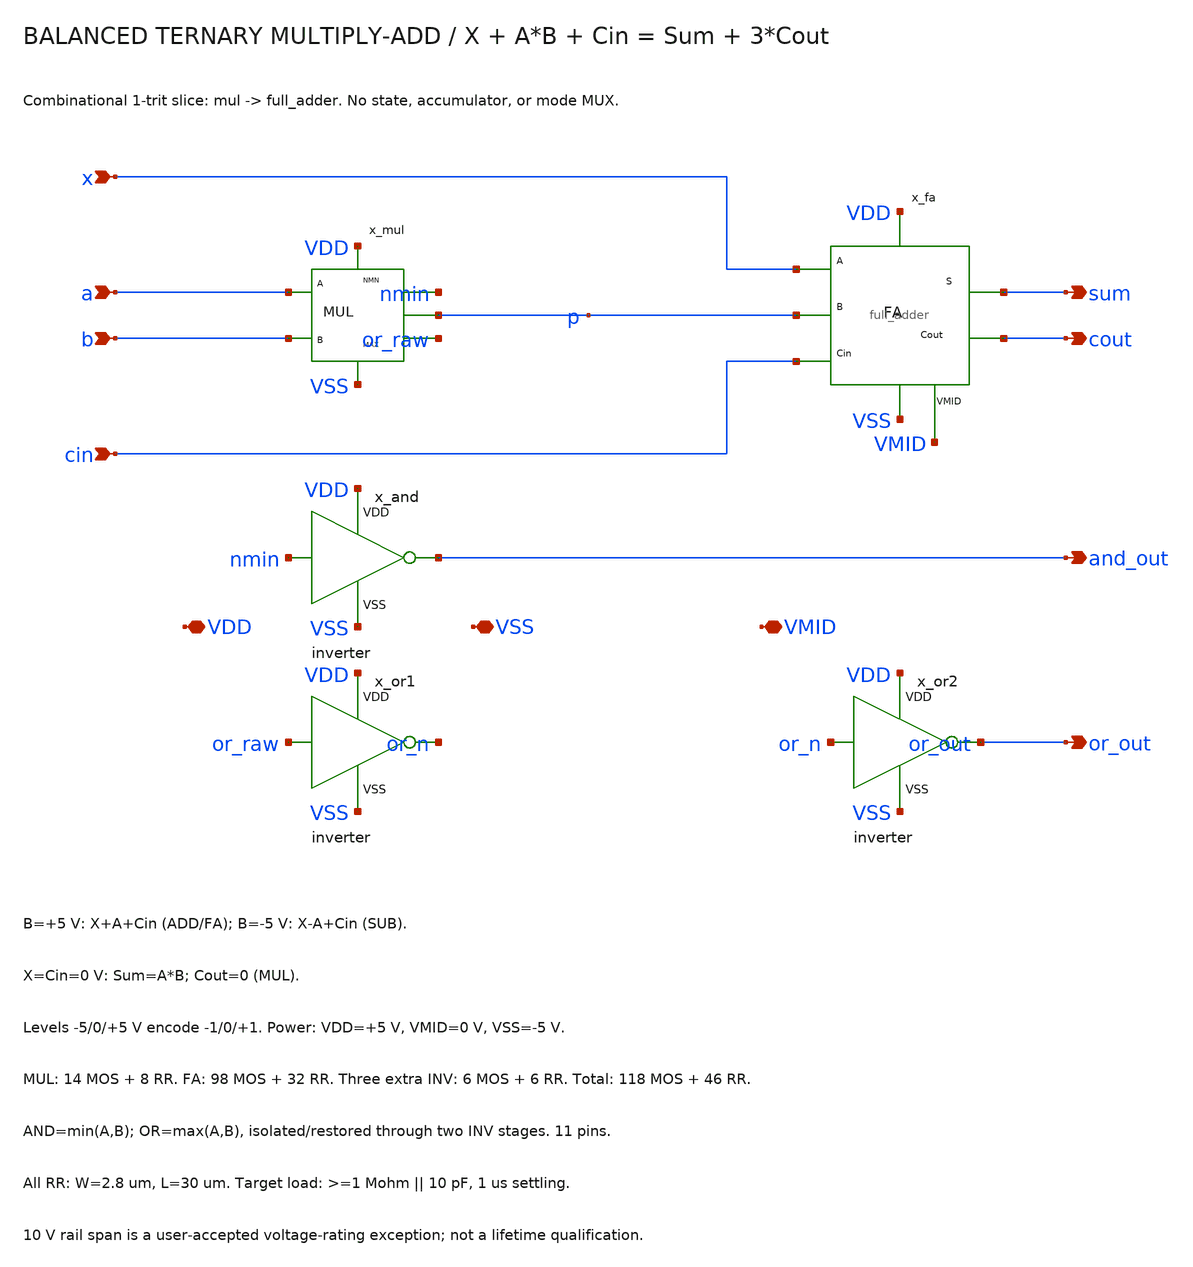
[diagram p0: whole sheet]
** sch_path: member_project/balanced-ternary-logic/PenguinEino/submission/mac.sch
**.subckt mac a b x cin sum cout and_out or_out VDD VSS VMID
*.ipin a
*.ipin b
*.ipin x
*.ipin cin
*.opin sum
*.opin cout
*.opin and_out
*.opin or_out
*.iopin VDD
*.iopin VSS
*.iopin VMID
x_mul a b p VDD VSS nmin or_raw mul
x_fa x p cin sum cout VDD VSS VMID full_adder
x_and nmin and_out VDD VSS inverter
x_or1 or_raw or_n VDD VSS inverter
x_or2 or_n or_out VDD VSS inverter
**.ends
.end
